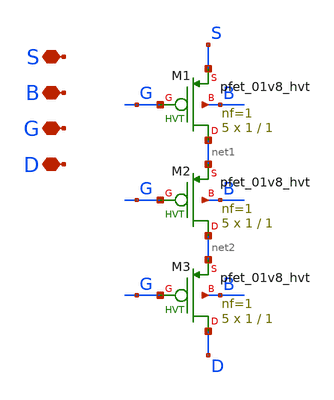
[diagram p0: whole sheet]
** sch_path: xschem/INA/Transistors/transistors_bias_network/pfet_m15.sch
**.subckt pfet_m15 S B G D
*.iopin S
*.iopin B
*.iopin G
*.iopin D
XM1 net1 G S B sky130_fd_pr__pfet_01v8_hvt L=1 W=1 nf=1 ad='int((nf+1)/2) * W/nf * 0.29' as='int((nf+2)/2) * W/nf * 0.29'
+ pd='2*int((nf+1)/2) * (W/nf + 0.29)' ps='2*int((nf+2)/2) * (W/nf + 0.29)' nrd='0.29 / W' nrs='0.29 / W'
+ sa=0 sb=0 sd=0 mult=5 m=5
XM2 net2 G net1 B sky130_fd_pr__pfet_01v8_hvt L=1 W=1 nf=1 ad='int((nf+1)/2) * W/nf * 0.29' as='int((nf+2)/2) * W/nf * 0.29'
+ pd='2*int((nf+1)/2) * (W/nf + 0.29)' ps='2*int((nf+2)/2) * (W/nf + 0.29)' nrd='0.29 / W' nrs='0.29 / W'
+ sa=0 sb=0 sd=0 mult=5 m=5
XM3 D G net2 B sky130_fd_pr__pfet_01v8_hvt L=1 W=1 nf=1 ad='int((nf+1)/2) * W/nf * 0.29' as='int((nf+2)/2) * W/nf * 0.29'
+ pd='2*int((nf+1)/2) * (W/nf + 0.29)' ps='2*int((nf+2)/2) * (W/nf + 0.29)' nrd='0.29 / W' nrs='0.29 / W'
+ sa=0 sb=0 sd=0 mult=5 m=5
**.ends
.end
